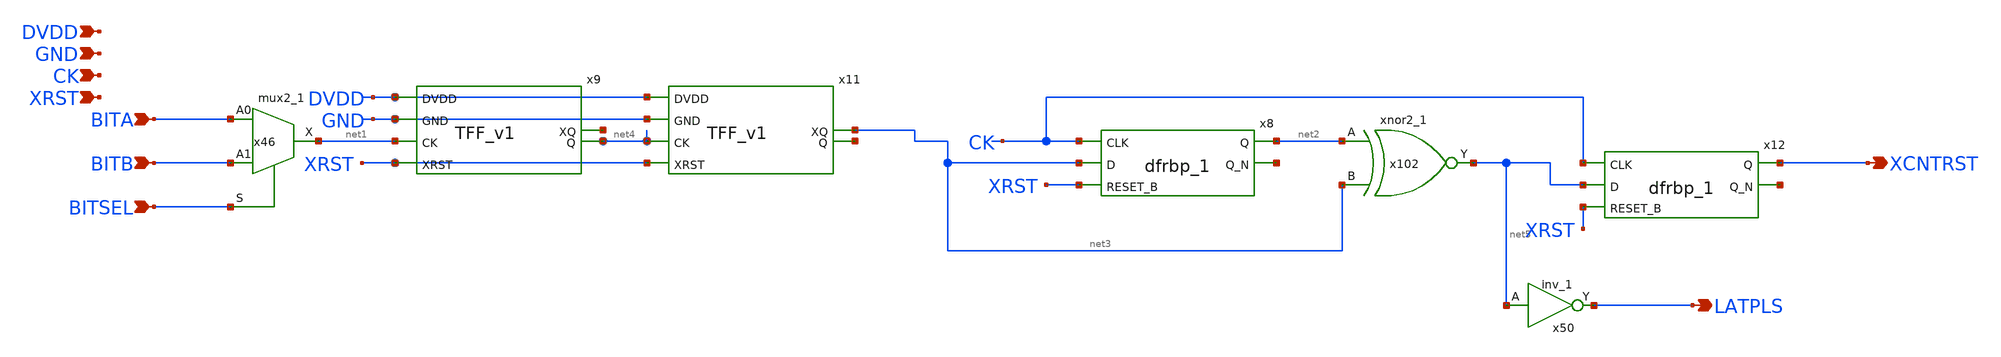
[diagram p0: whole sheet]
** sch_path: design/schematic/PLSGEN_v1.sch
**.subckt PLSGEN_v1 CK XRST DVDD GND BITA BITB BITSEL XCNTRST LATPLS
*.ipin CK
*.ipin XRST
*.ipin DVDD
*.ipin GND
*.ipin BITA
*.ipin BITB
*.ipin BITSEL
*.opin XCNTRST
*.opin LATPLS
x8 CK net3 XRST GND GND DVDD DVDD net2 net6 sky130_fd_sc_hd__dfrbp_1
x102 net2 net3 GND GND DVDD DVDD net5 sky130_fd_sc_hd__xnor2_1
x46 BITA BITB BITSEL GND GND DVDD DVDD net1 sky130_fd_sc_hd__mux2_1
x9 DVDD GND net7 net4 net1 XRST TFF_v1
x11 DVDD GND net3 net8 net4 XRST TFF_v1
x12 CK net5 XRST GND GND DVDD DVDD XCNTRST net9 sky130_fd_sc_hd__dfrbp_1
x50 net5 GND GND DVDD DVDD LATPLS sky130_fd_sc_hd__inv_1
**.ends

* expanding   symbol:  /home/ttuser/TT_WORK/rel/TFF_v1.sym # of pins=6
** sym_path: design/schematic/TFF_v1.sym
** sch_path: design/schematic/TFF_v1.sch
.subckt TFF_v1 DVDD GND XQ Q CK XRST
*.ipin CK
*.ipin XRST
*.opin XQ
*.opin Q
*.ipin DVDD
*.ipin GND
x0 CK XQ XRST GND GND DVDD DVDD Q XQ sky130_fd_sc_hd__dfrbp_1
.ends

.end
